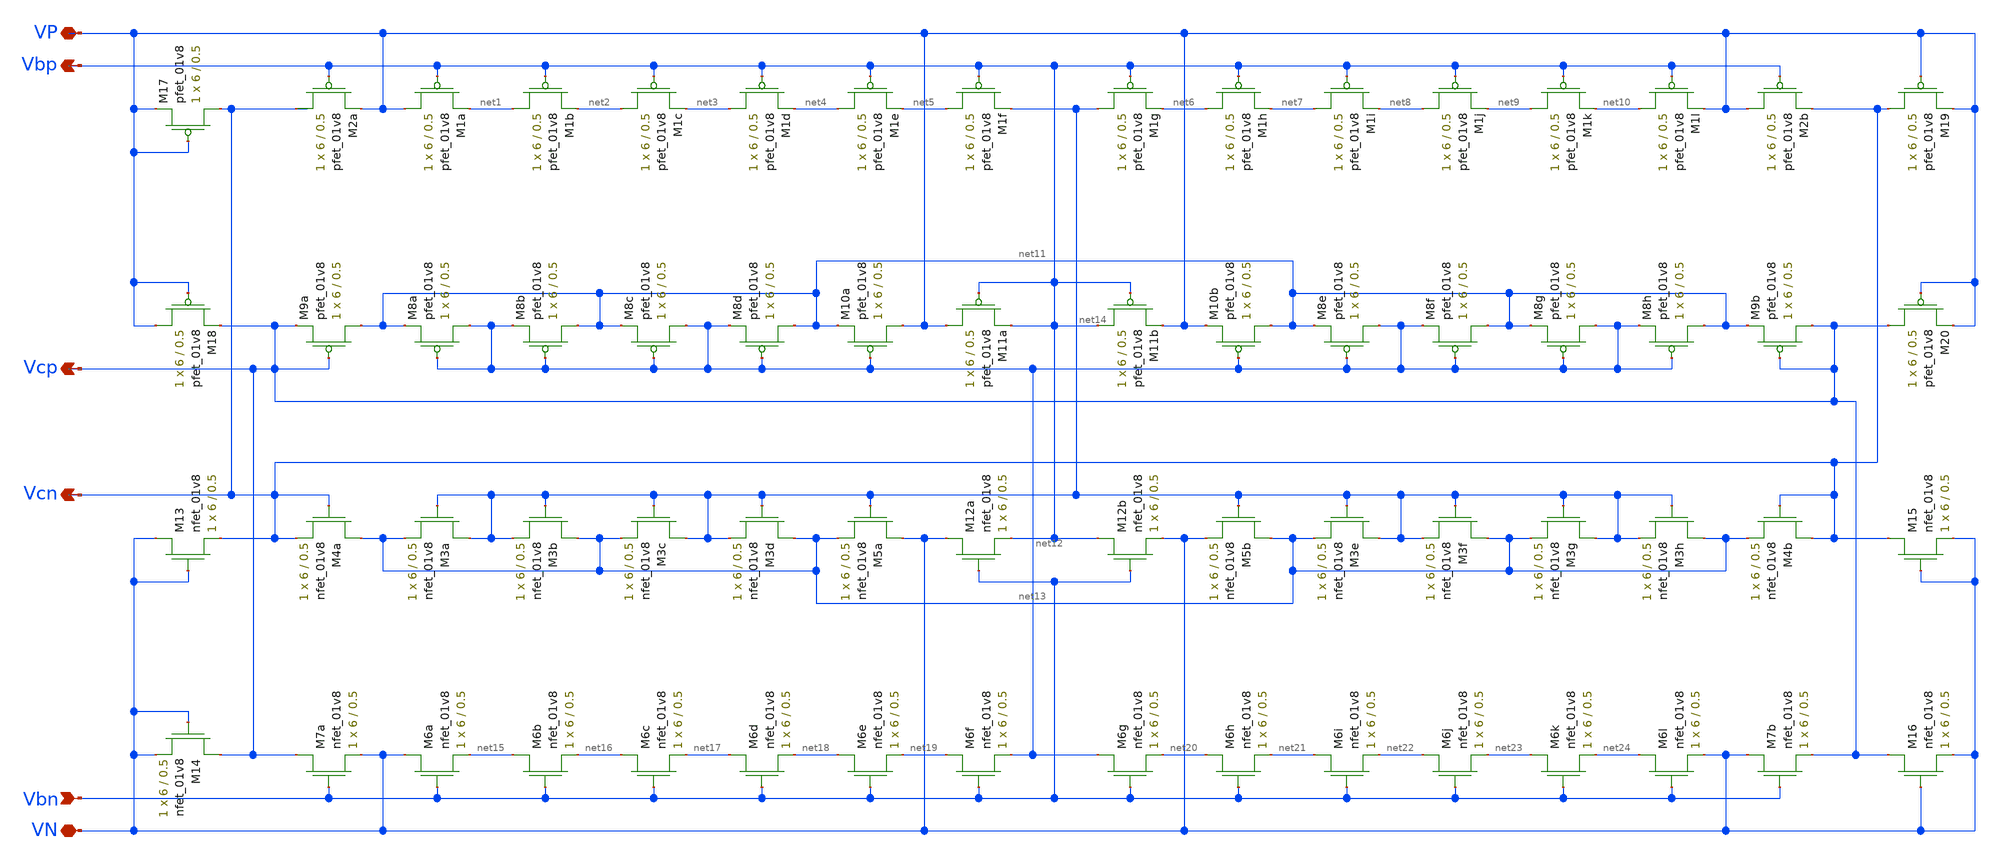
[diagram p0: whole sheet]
** sch_path: biasgen_lds.sch
**.subckt biasgen_lds Vbp VP Vcp Vcn Vbn VN
*.opin Vbp
*.iopin VP
*.opin Vcp
*.opin Vcn
*.ipin Vbn
*.iopin VN
XM2a Vcn Vbp VP VDD sky130_fd_pr__pfet_01v8 L=0.5 W=6 nf=1 ad='int((nf+1)/2) * W/nf * 0.29' as='int((nf+2)/2) * W/nf * 0.29'
+ pd='2*int((nf+1)/2) * (W/nf + 0.29)' ps='2*int((nf+2)/2) * (W/nf + 0.29)' nrd='0.29 / W' nrs='0.29 / W'
+ sa=0 sb=0 sd=0 mult=1 m=1
XM1a VP Vbp net1 VDD sky130_fd_pr__pfet_01v8 L=0.5 W=6 nf=1 ad='int((nf+1)/2) * W/nf * 0.29' as='int((nf+2)/2) * W/nf * 0.29'
+ pd='2*int((nf+1)/2) * (W/nf + 0.29)' ps='2*int((nf+2)/2) * (W/nf + 0.29)' nrd='0.29 / W' nrs='0.29 / W'
+ sa=0 sb=0 sd=0 mult=1 m=1
XM1b net1 Vbp net2 VDD sky130_fd_pr__pfet_01v8 L=0.5 W=6 nf=1 ad='int((nf+1)/2) * W/nf * 0.29' as='int((nf+2)/2) * W/nf * 0.29'
+ pd='2*int((nf+1)/2) * (W/nf + 0.29)' ps='2*int((nf+2)/2) * (W/nf + 0.29)' nrd='0.29 / W' nrs='0.29 / W'
+ sa=0 sb=0 sd=0 mult=1 m=1
XM1c net2 Vbp net3 VDD sky130_fd_pr__pfet_01v8 L=0.5 W=6 nf=1 ad='int((nf+1)/2) * W/nf * 0.29' as='int((nf+2)/2) * W/nf * 0.29'
+ pd='2*int((nf+1)/2) * (W/nf + 0.29)' ps='2*int((nf+2)/2) * (W/nf + 0.29)' nrd='0.29 / W' nrs='0.29 / W'
+ sa=0 sb=0 sd=0 mult=1 m=1
XM1d net3 Vbp net4 VDD sky130_fd_pr__pfet_01v8 L=0.5 W=6 nf=1 ad='int((nf+1)/2) * W/nf * 0.29' as='int((nf+2)/2) * W/nf * 0.29'
+ pd='2*int((nf+1)/2) * (W/nf + 0.29)' ps='2*int((nf+2)/2) * (W/nf + 0.29)' nrd='0.29 / W' nrs='0.29 / W'
+ sa=0 sb=0 sd=0 mult=1 m=1
XM1e net4 Vbp net5 VDD sky130_fd_pr__pfet_01v8 L=0.5 W=6 nf=1 ad='int((nf+1)/2) * W/nf * 0.29' as='int((nf+2)/2) * W/nf * 0.29'
+ pd='2*int((nf+1)/2) * (W/nf + 0.29)' ps='2*int((nf+2)/2) * (W/nf + 0.29)' nrd='0.29 / W' nrs='0.29 / W'
+ sa=0 sb=0 sd=0 mult=1 m=1
XM1f net5 Vbp net14 VDD sky130_fd_pr__pfet_01v8 L=0.5 W=6 nf=1 ad='int((nf+1)/2) * W/nf * 0.29' as='int((nf+2)/2) * W/nf * 0.29'
+ pd='2*int((nf+1)/2) * (W/nf + 0.29)' ps='2*int((nf+2)/2) * (W/nf + 0.29)' nrd='0.29 / W' nrs='0.29 / W'
+ sa=0 sb=0 sd=0 mult=1 m=1
XM1g net14 Vbp net6 VDD sky130_fd_pr__pfet_01v8 L=0.5 W=6 nf=1 ad='int((nf+1)/2) * W/nf * 0.29' as='int((nf+2)/2) * W/nf * 0.29'
+ pd='2*int((nf+1)/2) * (W/nf + 0.29)' ps='2*int((nf+2)/2) * (W/nf + 0.29)' nrd='0.29 / W' nrs='0.29 / W'
+ sa=0 sb=0 sd=0 mult=1 m=1
XM1h net6 Vbp net7 VDD sky130_fd_pr__pfet_01v8 L=0.5 W=6 nf=1 ad='int((nf+1)/2) * W/nf * 0.29' as='int((nf+2)/2) * W/nf * 0.29'
+ pd='2*int((nf+1)/2) * (W/nf + 0.29)' ps='2*int((nf+2)/2) * (W/nf + 0.29)' nrd='0.29 / W' nrs='0.29 / W'
+ sa=0 sb=0 sd=0 mult=1 m=1
XM1i net7 Vbp net8 VDD sky130_fd_pr__pfet_01v8 L=0.5 W=6 nf=1 ad='int((nf+1)/2) * W/nf * 0.29' as='int((nf+2)/2) * W/nf * 0.29'
+ pd='2*int((nf+1)/2) * (W/nf + 0.29)' ps='2*int((nf+2)/2) * (W/nf + 0.29)' nrd='0.29 / W' nrs='0.29 / W'
+ sa=0 sb=0 sd=0 mult=1 m=1
XM1j net8 Vbp net9 VDD sky130_fd_pr__pfet_01v8 L=0.5 W=6 nf=1 ad='int((nf+1)/2) * W/nf * 0.29' as='int((nf+2)/2) * W/nf * 0.29'
+ pd='2*int((nf+1)/2) * (W/nf + 0.29)' ps='2*int((nf+2)/2) * (W/nf + 0.29)' nrd='0.29 / W' nrs='0.29 / W'
+ sa=0 sb=0 sd=0 mult=1 m=1
XM1k net9 Vbp net10 VDD sky130_fd_pr__pfet_01v8 L=0.5 W=6 nf=1 ad='int((nf+1)/2) * W/nf * 0.29' as='int((nf+2)/2) * W/nf * 0.29'
+ pd='2*int((nf+1)/2) * (W/nf + 0.29)' ps='2*int((nf+2)/2) * (W/nf + 0.29)' nrd='0.29 / W' nrs='0.29 / W'
+ sa=0 sb=0 sd=0 mult=1 m=1
XM1l net10 Vbp VP VDD sky130_fd_pr__pfet_01v8 L=0.5 W=6 nf=1 ad='int((nf+1)/2) * W/nf * 0.29' as='int((nf+2)/2) * W/nf * 0.29'
+ pd='2*int((nf+1)/2) * (W/nf + 0.29)' ps='2*int((nf+2)/2) * (W/nf + 0.29)' nrd='0.29 / W' nrs='0.29 / W'
+ sa=0 sb=0 sd=0 mult=1 m=1
XM2b VP Vbp Vcn VDD sky130_fd_pr__pfet_01v8 L=0.5 W=6 nf=1 ad='int((nf+1)/2) * W/nf * 0.29' as='int((nf+2)/2) * W/nf * 0.29'
+ pd='2*int((nf+1)/2) * (W/nf + 0.29)' ps='2*int((nf+2)/2) * (W/nf + 0.29)' nrd='0.29 / W' nrs='0.29 / W'
+ sa=0 sb=0 sd=0 mult=1 m=1
XM9a net11 Vcp Vcp VDD sky130_fd_pr__pfet_01v8 L=0.5 W=6 nf=1 ad='int((nf+1)/2) * W/nf * 0.29' as='int((nf+2)/2) * W/nf * 0.29'
+ pd='2*int((nf+1)/2) * (W/nf + 0.29)' ps='2*int((nf+2)/2) * (W/nf + 0.29)' nrd='0.29 / W' nrs='0.29 / W'
+ sa=0 sb=0 sd=0 mult=1 m=1
XM8a net12 net12 net11 VDD sky130_fd_pr__pfet_01v8 L=0.5 W=6 nf=1 ad='int((nf+1)/2) * W/nf * 0.29' as='int((nf+2)/2) * W/nf * 0.29'
+ pd='2*int((nf+1)/2) * (W/nf + 0.29)' ps='2*int((nf+2)/2) * (W/nf + 0.29)' nrd='0.29 / W' nrs='0.29 / W'
+ sa=0 sb=0 sd=0 mult=1 m=1
XM8b net11 net12 net12 VDD sky130_fd_pr__pfet_01v8 L=0.5 W=6 nf=1 ad='int((nf+1)/2) * W/nf * 0.29' as='int((nf+2)/2) * W/nf * 0.29'
+ pd='2*int((nf+1)/2) * (W/nf + 0.29)' ps='2*int((nf+2)/2) * (W/nf + 0.29)' nrd='0.29 / W' nrs='0.29 / W'
+ sa=0 sb=0 sd=0 mult=1 m=1
XM8c net12 net12 net11 VDD sky130_fd_pr__pfet_01v8 L=0.5 W=6 nf=1 ad='int((nf+1)/2) * W/nf * 0.29' as='int((nf+2)/2) * W/nf * 0.29'
+ pd='2*int((nf+1)/2) * (W/nf + 0.29)' ps='2*int((nf+2)/2) * (W/nf + 0.29)' nrd='0.29 / W' nrs='0.29 / W'
+ sa=0 sb=0 sd=0 mult=1 m=1
XM8d net11 net12 net12 VDD sky130_fd_pr__pfet_01v8 L=0.5 W=6 nf=1 ad='int((nf+1)/2) * W/nf * 0.29' as='int((nf+2)/2) * W/nf * 0.29'
+ pd='2*int((nf+1)/2) * (W/nf + 0.29)' ps='2*int((nf+2)/2) * (W/nf + 0.29)' nrd='0.29 / W' nrs='0.29 / W'
+ sa=0 sb=0 sd=0 mult=1 m=1
XM10a VP net12 net11 VDD sky130_fd_pr__pfet_01v8 L=0.5 W=6 nf=1 ad='int((nf+1)/2) * W/nf * 0.29' as='int((nf+2)/2) * W/nf * 0.29'
+ pd='2*int((nf+1)/2) * (W/nf + 0.29)' ps='2*int((nf+2)/2) * (W/nf + 0.29)' nrd='0.29 / W' nrs='0.29 / W'
+ sa=0 sb=0 sd=0 mult=1 m=1
XM11a VP Vbp Vbp VDD sky130_fd_pr__pfet_01v8 L=0.5 W=6 nf=1 ad='int((nf+1)/2) * W/nf * 0.29' as='int((nf+2)/2) * W/nf * 0.29'
+ pd='2*int((nf+1)/2) * (W/nf + 0.29)' ps='2*int((nf+2)/2) * (W/nf + 0.29)' nrd='0.29 / W' nrs='0.29 / W'
+ sa=0 sb=0 sd=0 mult=1 m=1
XM11b Vbp Vbp VP VDD sky130_fd_pr__pfet_01v8 L=0.5 W=6 nf=1 ad='int((nf+1)/2) * W/nf * 0.29' as='int((nf+2)/2) * W/nf * 0.29'
+ pd='2*int((nf+1)/2) * (W/nf + 0.29)' ps='2*int((nf+2)/2) * (W/nf + 0.29)' nrd='0.29 / W' nrs='0.29 / W'
+ sa=0 sb=0 sd=0 mult=1 m=1
XM10b net11 net12 VP VDD sky130_fd_pr__pfet_01v8 L=0.5 W=6 nf=1 ad='int((nf+1)/2) * W/nf * 0.29' as='int((nf+2)/2) * W/nf * 0.29'
+ pd='2*int((nf+1)/2) * (W/nf + 0.29)' ps='2*int((nf+2)/2) * (W/nf + 0.29)' nrd='0.29 / W' nrs='0.29 / W'
+ sa=0 sb=0 sd=0 mult=1 m=1
XM8e net12 net12 net11 VDD sky130_fd_pr__pfet_01v8 L=0.5 W=6 nf=1 ad='int((nf+1)/2) * W/nf * 0.29' as='int((nf+2)/2) * W/nf * 0.29'
+ pd='2*int((nf+1)/2) * (W/nf + 0.29)' ps='2*int((nf+2)/2) * (W/nf + 0.29)' nrd='0.29 / W' nrs='0.29 / W'
+ sa=0 sb=0 sd=0 mult=1 m=1
XM8f net11 net12 net12 VDD sky130_fd_pr__pfet_01v8 L=0.5 W=6 nf=1 ad='int((nf+1)/2) * W/nf * 0.29' as='int((nf+2)/2) * W/nf * 0.29'
+ pd='2*int((nf+1)/2) * (W/nf + 0.29)' ps='2*int((nf+2)/2) * (W/nf + 0.29)' nrd='0.29 / W' nrs='0.29 / W'
+ sa=0 sb=0 sd=0 mult=1 m=1
XM8g net12 net12 net11 VDD sky130_fd_pr__pfet_01v8 L=0.5 W=6 nf=1 ad='int((nf+1)/2) * W/nf * 0.29' as='int((nf+2)/2) * W/nf * 0.29'
+ pd='2*int((nf+1)/2) * (W/nf + 0.29)' ps='2*int((nf+2)/2) * (W/nf + 0.29)' nrd='0.29 / W' nrs='0.29 / W'
+ sa=0 sb=0 sd=0 mult=1 m=1
XM8h net11 net12 net12 VDD sky130_fd_pr__pfet_01v8 L=0.5 W=6 nf=1 ad='int((nf+1)/2) * W/nf * 0.29' as='int((nf+2)/2) * W/nf * 0.29'
+ pd='2*int((nf+1)/2) * (W/nf + 0.29)' ps='2*int((nf+2)/2) * (W/nf + 0.29)' nrd='0.29 / W' nrs='0.29 / W'
+ sa=0 sb=0 sd=0 mult=1 m=1
XM9b Vcp Vcp net11 VDD sky130_fd_pr__pfet_01v8 L=0.5 W=6 nf=1 ad='int((nf+1)/2) * W/nf * 0.29' as='int((nf+2)/2) * W/nf * 0.29'
+ pd='2*int((nf+1)/2) * (W/nf + 0.29)' ps='2*int((nf+2)/2) * (W/nf + 0.29)' nrd='0.29 / W' nrs='0.29 / W'
+ sa=0 sb=0 sd=0 mult=1 m=1
XM4a net13 Vcn Vcn GND sky130_fd_pr__nfet_01v8 L=0.5 W=6 nf=1 ad='int((nf+1)/2) * W/nf * 0.29' as='int((nf+2)/2) * W/nf * 0.29'
+ pd='2*int((nf+1)/2) * (W/nf + 0.29)' ps='2*int((nf+2)/2) * (W/nf + 0.29)' nrd='0.29 / W' nrs='0.29 / W'
+ sa=0 sb=0 sd=0 mult=1 m=1
XM3a net14 net14 net13 GND sky130_fd_pr__nfet_01v8 L=0.5 W=6 nf=1 ad='int((nf+1)/2) * W/nf * 0.29' as='int((nf+2)/2) * W/nf * 0.29'
+ pd='2*int((nf+1)/2) * (W/nf + 0.29)' ps='2*int((nf+2)/2) * (W/nf + 0.29)' nrd='0.29 / W' nrs='0.29 / W'
+ sa=0 sb=0 sd=0 mult=1 m=1
XM3b net13 net14 net14 GND sky130_fd_pr__nfet_01v8 L=0.5 W=6 nf=1 ad='int((nf+1)/2) * W/nf * 0.29' as='int((nf+2)/2) * W/nf * 0.29'
+ pd='2*int((nf+1)/2) * (W/nf + 0.29)' ps='2*int((nf+2)/2) * (W/nf + 0.29)' nrd='0.29 / W' nrs='0.29 / W'
+ sa=0 sb=0 sd=0 mult=1 m=1
XM3c net14 net14 net13 GND sky130_fd_pr__nfet_01v8 L=0.5 W=6 nf=1 ad='int((nf+1)/2) * W/nf * 0.29' as='int((nf+2)/2) * W/nf * 0.29'
+ pd='2*int((nf+1)/2) * (W/nf + 0.29)' ps='2*int((nf+2)/2) * (W/nf + 0.29)' nrd='0.29 / W' nrs='0.29 / W'
+ sa=0 sb=0 sd=0 mult=1 m=1
XM3d net13 net14 net14 GND sky130_fd_pr__nfet_01v8 L=0.5 W=6 nf=1 ad='int((nf+1)/2) * W/nf * 0.29' as='int((nf+2)/2) * W/nf * 0.29'
+ pd='2*int((nf+1)/2) * (W/nf + 0.29)' ps='2*int((nf+2)/2) * (W/nf + 0.29)' nrd='0.29 / W' nrs='0.29 / W'
+ sa=0 sb=0 sd=0 mult=1 m=1
XM5a VN net14 net13 GND sky130_fd_pr__nfet_01v8 L=0.5 W=6 nf=1 ad='int((nf+1)/2) * W/nf * 0.29' as='int((nf+2)/2) * W/nf * 0.29'
+ pd='2*int((nf+1)/2) * (W/nf + 0.29)' ps='2*int((nf+2)/2) * (W/nf + 0.29)' nrd='0.29 / W' nrs='0.29 / W'
+ sa=0 sb=0 sd=0 mult=1 m=1
XM12a VN Vbn Vbp GND sky130_fd_pr__nfet_01v8 L=0.5 W=6 nf=1 ad='int((nf+1)/2) * W/nf * 0.29' as='int((nf+2)/2) * W/nf * 0.29'
+ pd='2*int((nf+1)/2) * (W/nf + 0.29)' ps='2*int((nf+2)/2) * (W/nf + 0.29)' nrd='0.29 / W' nrs='0.29 / W'
+ sa=0 sb=0 sd=0 mult=1 m=1
XM12b Vbp Vbn VN GND sky130_fd_pr__nfet_01v8 L=0.5 W=6 nf=1 ad='int((nf+1)/2) * W/nf * 0.29' as='int((nf+2)/2) * W/nf * 0.29'
+ pd='2*int((nf+1)/2) * (W/nf + 0.29)' ps='2*int((nf+2)/2) * (W/nf + 0.29)' nrd='0.29 / W' nrs='0.29 / W'
+ sa=0 sb=0 sd=0 mult=1 m=1
XM5b net13 net14 VN GND sky130_fd_pr__nfet_01v8 L=0.5 W=6 nf=1 ad='int((nf+1)/2) * W/nf * 0.29' as='int((nf+2)/2) * W/nf * 0.29'
+ pd='2*int((nf+1)/2) * (W/nf + 0.29)' ps='2*int((nf+2)/2) * (W/nf + 0.29)' nrd='0.29 / W' nrs='0.29 / W'
+ sa=0 sb=0 sd=0 mult=1 m=1
XM3e net14 net14 net13 GND sky130_fd_pr__nfet_01v8 L=0.5 W=6 nf=1 ad='int((nf+1)/2) * W/nf * 0.29' as='int((nf+2)/2) * W/nf * 0.29'
+ pd='2*int((nf+1)/2) * (W/nf + 0.29)' ps='2*int((nf+2)/2) * (W/nf + 0.29)' nrd='0.29 / W' nrs='0.29 / W'
+ sa=0 sb=0 sd=0 mult=1 m=1
XM3f net13 net14 net14 GND sky130_fd_pr__nfet_01v8 L=0.5 W=6 nf=1 ad='int((nf+1)/2) * W/nf * 0.29' as='int((nf+2)/2) * W/nf * 0.29'
+ pd='2*int((nf+1)/2) * (W/nf + 0.29)' ps='2*int((nf+2)/2) * (W/nf + 0.29)' nrd='0.29 / W' nrs='0.29 / W'
+ sa=0 sb=0 sd=0 mult=1 m=1
XM3g net14 net14 net13 GND sky130_fd_pr__nfet_01v8 L=0.5 W=6 nf=1 ad='int((nf+1)/2) * W/nf * 0.29' as='int((nf+2)/2) * W/nf * 0.29'
+ pd='2*int((nf+1)/2) * (W/nf + 0.29)' ps='2*int((nf+2)/2) * (W/nf + 0.29)' nrd='0.29 / W' nrs='0.29 / W'
+ sa=0 sb=0 sd=0 mult=1 m=1
XM3h net13 net14 net14 GND sky130_fd_pr__nfet_01v8 L=0.5 W=6 nf=1 ad='int((nf+1)/2) * W/nf * 0.29' as='int((nf+2)/2) * W/nf * 0.29'
+ pd='2*int((nf+1)/2) * (W/nf + 0.29)' ps='2*int((nf+2)/2) * (W/nf + 0.29)' nrd='0.29 / W' nrs='0.29 / W'
+ sa=0 sb=0 sd=0 mult=1 m=1
XM4b Vcn Vcn net13 GND sky130_fd_pr__nfet_01v8 L=0.5 W=6 nf=1 ad='int((nf+1)/2) * W/nf * 0.29' as='int((nf+2)/2) * W/nf * 0.29'
+ pd='2*int((nf+1)/2) * (W/nf + 0.29)' ps='2*int((nf+2)/2) * (W/nf + 0.29)' nrd='0.29 / W' nrs='0.29 / W'
+ sa=0 sb=0 sd=0 mult=1 m=1
XM7a Vcp Vbn VN GND sky130_fd_pr__nfet_01v8 L=0.5 W=6 nf=1 ad='int((nf+1)/2) * W/nf * 0.29' as='int((nf+2)/2) * W/nf * 0.29'
+ pd='2*int((nf+1)/2) * (W/nf + 0.29)' ps='2*int((nf+2)/2) * (W/nf + 0.29)' nrd='0.29 / W' nrs='0.29 / W'
+ sa=0 sb=0 sd=0 mult=1 m=1
XM6a VN Vbn net15 GND sky130_fd_pr__nfet_01v8 L=0.5 W=6 nf=1 ad='int((nf+1)/2) * W/nf * 0.29' as='int((nf+2)/2) * W/nf * 0.29'
+ pd='2*int((nf+1)/2) * (W/nf + 0.29)' ps='2*int((nf+2)/2) * (W/nf + 0.29)' nrd='0.29 / W' nrs='0.29 / W'
+ sa=0 sb=0 sd=0 mult=1 m=1
XM6b net15 Vbn net16 GND sky130_fd_pr__nfet_01v8 L=0.5 W=6 nf=1 ad='int((nf+1)/2) * W/nf * 0.29' as='int((nf+2)/2) * W/nf * 0.29'
+ pd='2*int((nf+1)/2) * (W/nf + 0.29)' ps='2*int((nf+2)/2) * (W/nf + 0.29)' nrd='0.29 / W' nrs='0.29 / W'
+ sa=0 sb=0 sd=0 mult=1 m=1
XM6c net16 Vbn net17 GND sky130_fd_pr__nfet_01v8 L=0.5 W=6 nf=1 ad='int((nf+1)/2) * W/nf * 0.29' as='int((nf+2)/2) * W/nf * 0.29'
+ pd='2*int((nf+1)/2) * (W/nf + 0.29)' ps='2*int((nf+2)/2) * (W/nf + 0.29)' nrd='0.29 / W' nrs='0.29 / W'
+ sa=0 sb=0 sd=0 mult=1 m=1
XM6d net17 Vbn net18 GND sky130_fd_pr__nfet_01v8 L=0.5 W=6 nf=1 ad='int((nf+1)/2) * W/nf * 0.29' as='int((nf+2)/2) * W/nf * 0.29'
+ pd='2*int((nf+1)/2) * (W/nf + 0.29)' ps='2*int((nf+2)/2) * (W/nf + 0.29)' nrd='0.29 / W' nrs='0.29 / W'
+ sa=0 sb=0 sd=0 mult=1 m=1
XM6e net18 Vbn net19 GND sky130_fd_pr__nfet_01v8 L=0.5 W=6 nf=1 ad='int((nf+1)/2) * W/nf * 0.29' as='int((nf+2)/2) * W/nf * 0.29'
+ pd='2*int((nf+1)/2) * (W/nf + 0.29)' ps='2*int((nf+2)/2) * (W/nf + 0.29)' nrd='0.29 / W' nrs='0.29 / W'
+ sa=0 sb=0 sd=0 mult=1 m=1
XM6f net19 Vbn net12 GND sky130_fd_pr__nfet_01v8 L=0.5 W=6 nf=1 ad='int((nf+1)/2) * W/nf * 0.29' as='int((nf+2)/2) * W/nf * 0.29'
+ pd='2*int((nf+1)/2) * (W/nf + 0.29)' ps='2*int((nf+2)/2) * (W/nf + 0.29)' nrd='0.29 / W' nrs='0.29 / W'
+ sa=0 sb=0 sd=0 mult=1 m=1
XM6g net12 Vbn net20 GND sky130_fd_pr__nfet_01v8 L=0.5 W=6 nf=1 ad='int((nf+1)/2) * W/nf * 0.29' as='int((nf+2)/2) * W/nf * 0.29'
+ pd='2*int((nf+1)/2) * (W/nf + 0.29)' ps='2*int((nf+2)/2) * (W/nf + 0.29)' nrd='0.29 / W' nrs='0.29 / W'
+ sa=0 sb=0 sd=0 mult=1 m=1
XM6h net20 Vbn net21 GND sky130_fd_pr__nfet_01v8 L=0.5 W=6 nf=1 ad='int((nf+1)/2) * W/nf * 0.29' as='int((nf+2)/2) * W/nf * 0.29'
+ pd='2*int((nf+1)/2) * (W/nf + 0.29)' ps='2*int((nf+2)/2) * (W/nf + 0.29)' nrd='0.29 / W' nrs='0.29 / W'
+ sa=0 sb=0 sd=0 mult=1 m=1
XM6i net21 Vbn net22 GND sky130_fd_pr__nfet_01v8 L=0.5 W=6 nf=1 ad='int((nf+1)/2) * W/nf * 0.29' as='int((nf+2)/2) * W/nf * 0.29'
+ pd='2*int((nf+1)/2) * (W/nf + 0.29)' ps='2*int((nf+2)/2) * (W/nf + 0.29)' nrd='0.29 / W' nrs='0.29 / W'
+ sa=0 sb=0 sd=0 mult=1 m=1
XM6j net22 Vbn net23 GND sky130_fd_pr__nfet_01v8 L=0.5 W=6 nf=1 ad='int((nf+1)/2) * W/nf * 0.29' as='int((nf+2)/2) * W/nf * 0.29'
+ pd='2*int((nf+1)/2) * (W/nf + 0.29)' ps='2*int((nf+2)/2) * (W/nf + 0.29)' nrd='0.29 / W' nrs='0.29 / W'
+ sa=0 sb=0 sd=0 mult=1 m=1
XM6k net23 Vbn net24 GND sky130_fd_pr__nfet_01v8 L=0.5 W=6 nf=1 ad='int((nf+1)/2) * W/nf * 0.29' as='int((nf+2)/2) * W/nf * 0.29'
+ pd='2*int((nf+1)/2) * (W/nf + 0.29)' ps='2*int((nf+2)/2) * (W/nf + 0.29)' nrd='0.29 / W' nrs='0.29 / W'
+ sa=0 sb=0 sd=0 mult=1 m=1
XM6l net24 Vbn VN GND sky130_fd_pr__nfet_01v8 L=0.5 W=6 nf=1 ad='int((nf+1)/2) * W/nf * 0.29' as='int((nf+2)/2) * W/nf * 0.29'
+ pd='2*int((nf+1)/2) * (W/nf + 0.29)' ps='2*int((nf+2)/2) * (W/nf + 0.29)' nrd='0.29 / W' nrs='0.29 / W'
+ sa=0 sb=0 sd=0 mult=1 m=1
XM7b VN Vbn Vcp GND sky130_fd_pr__nfet_01v8 L=0.5 W=6 nf=1 ad='int((nf+1)/2) * W/nf * 0.29' as='int((nf+2)/2) * W/nf * 0.29'
+ pd='2*int((nf+1)/2) * (W/nf + 0.29)' ps='2*int((nf+2)/2) * (W/nf + 0.29)' nrd='0.29 / W' nrs='0.29 / W'
+ sa=0 sb=0 sd=0 mult=1 m=1
XM17 Vcn VP VP VDD sky130_fd_pr__pfet_01v8 L=0.5 W=6 nf=1 ad='int((nf+1)/2) * W/nf * 0.29' as='int((nf+2)/2) * W/nf * 0.29'
+ pd='2*int((nf+1)/2) * (W/nf + 0.29)' ps='2*int((nf+2)/2) * (W/nf + 0.29)' nrd='0.29 / W' nrs='0.29 / W'
+ sa=0 sb=0 sd=0 mult=1 m=1
XM18 VP VP Vcp VDD sky130_fd_pr__pfet_01v8 L=0.5 W=6 nf=1 ad='int((nf+1)/2) * W/nf * 0.29' as='int((nf+2)/2) * W/nf * 0.29'
+ pd='2*int((nf+1)/2) * (W/nf + 0.29)' ps='2*int((nf+2)/2) * (W/nf + 0.29)' nrd='0.29 / W' nrs='0.29 / W'
+ sa=0 sb=0 sd=0 mult=1 m=1
XM13 VN VN Vcn GND sky130_fd_pr__nfet_01v8 L=0.5 W=6 nf=1 ad='int((nf+1)/2) * W/nf * 0.29' as='int((nf+2)/2) * W/nf * 0.29'
+ pd='2*int((nf+1)/2) * (W/nf + 0.29)' ps='2*int((nf+2)/2) * (W/nf + 0.29)' nrd='0.29 / W' nrs='0.29 / W'
+ sa=0 sb=0 sd=0 mult=1 m=1
XM14 Vcp VN VN GND sky130_fd_pr__nfet_01v8 L=0.5 W=6 nf=1 ad='int((nf+1)/2) * W/nf * 0.29' as='int((nf+2)/2) * W/nf * 0.29'
+ pd='2*int((nf+1)/2) * (W/nf + 0.29)' ps='2*int((nf+2)/2) * (W/nf + 0.29)' nrd='0.29 / W' nrs='0.29 / W'
+ sa=0 sb=0 sd=0 mult=1 m=1
XM19 Vcn VP VP VDD sky130_fd_pr__pfet_01v8 L=0.5 W=6 nf=1 ad='int((nf+1)/2) * W/nf * 0.29' as='int((nf+2)/2) * W/nf * 0.29'
+ pd='2*int((nf+1)/2) * (W/nf + 0.29)' ps='2*int((nf+2)/2) * (W/nf + 0.29)' nrd='0.29 / W' nrs='0.29 / W'
+ sa=0 sb=0 sd=0 mult=1 m=1
XM20 Vcp VP VP VDD sky130_fd_pr__pfet_01v8 L=0.5 W=6 nf=1 ad='int((nf+1)/2) * W/nf * 0.29' as='int((nf+2)/2) * W/nf * 0.29'
+ pd='2*int((nf+1)/2) * (W/nf + 0.29)' ps='2*int((nf+2)/2) * (W/nf + 0.29)' nrd='0.29 / W' nrs='0.29 / W'
+ sa=0 sb=0 sd=0 mult=1 m=1
XM15 Vcn VN VN GND sky130_fd_pr__nfet_01v8 L=0.5 W=6 nf=1 ad='int((nf+1)/2) * W/nf * 0.29' as='int((nf+2)/2) * W/nf * 0.29'
+ pd='2*int((nf+1)/2) * (W/nf + 0.29)' ps='2*int((nf+2)/2) * (W/nf + 0.29)' nrd='0.29 / W' nrs='0.29 / W'
+ sa=0 sb=0 sd=0 mult=1 m=1
XM16 Vcp VN VN GND sky130_fd_pr__nfet_01v8 L=0.5 W=6 nf=1 ad='int((nf+1)/2) * W/nf * 0.29' as='int((nf+2)/2) * W/nf * 0.29'
+ pd='2*int((nf+1)/2) * (W/nf + 0.29)' ps='2*int((nf+2)/2) * (W/nf + 0.29)' nrd='0.29 / W' nrs='0.29 / W'
+ sa=0 sb=0 sd=0 mult=1 m=1
**.ends
.end
